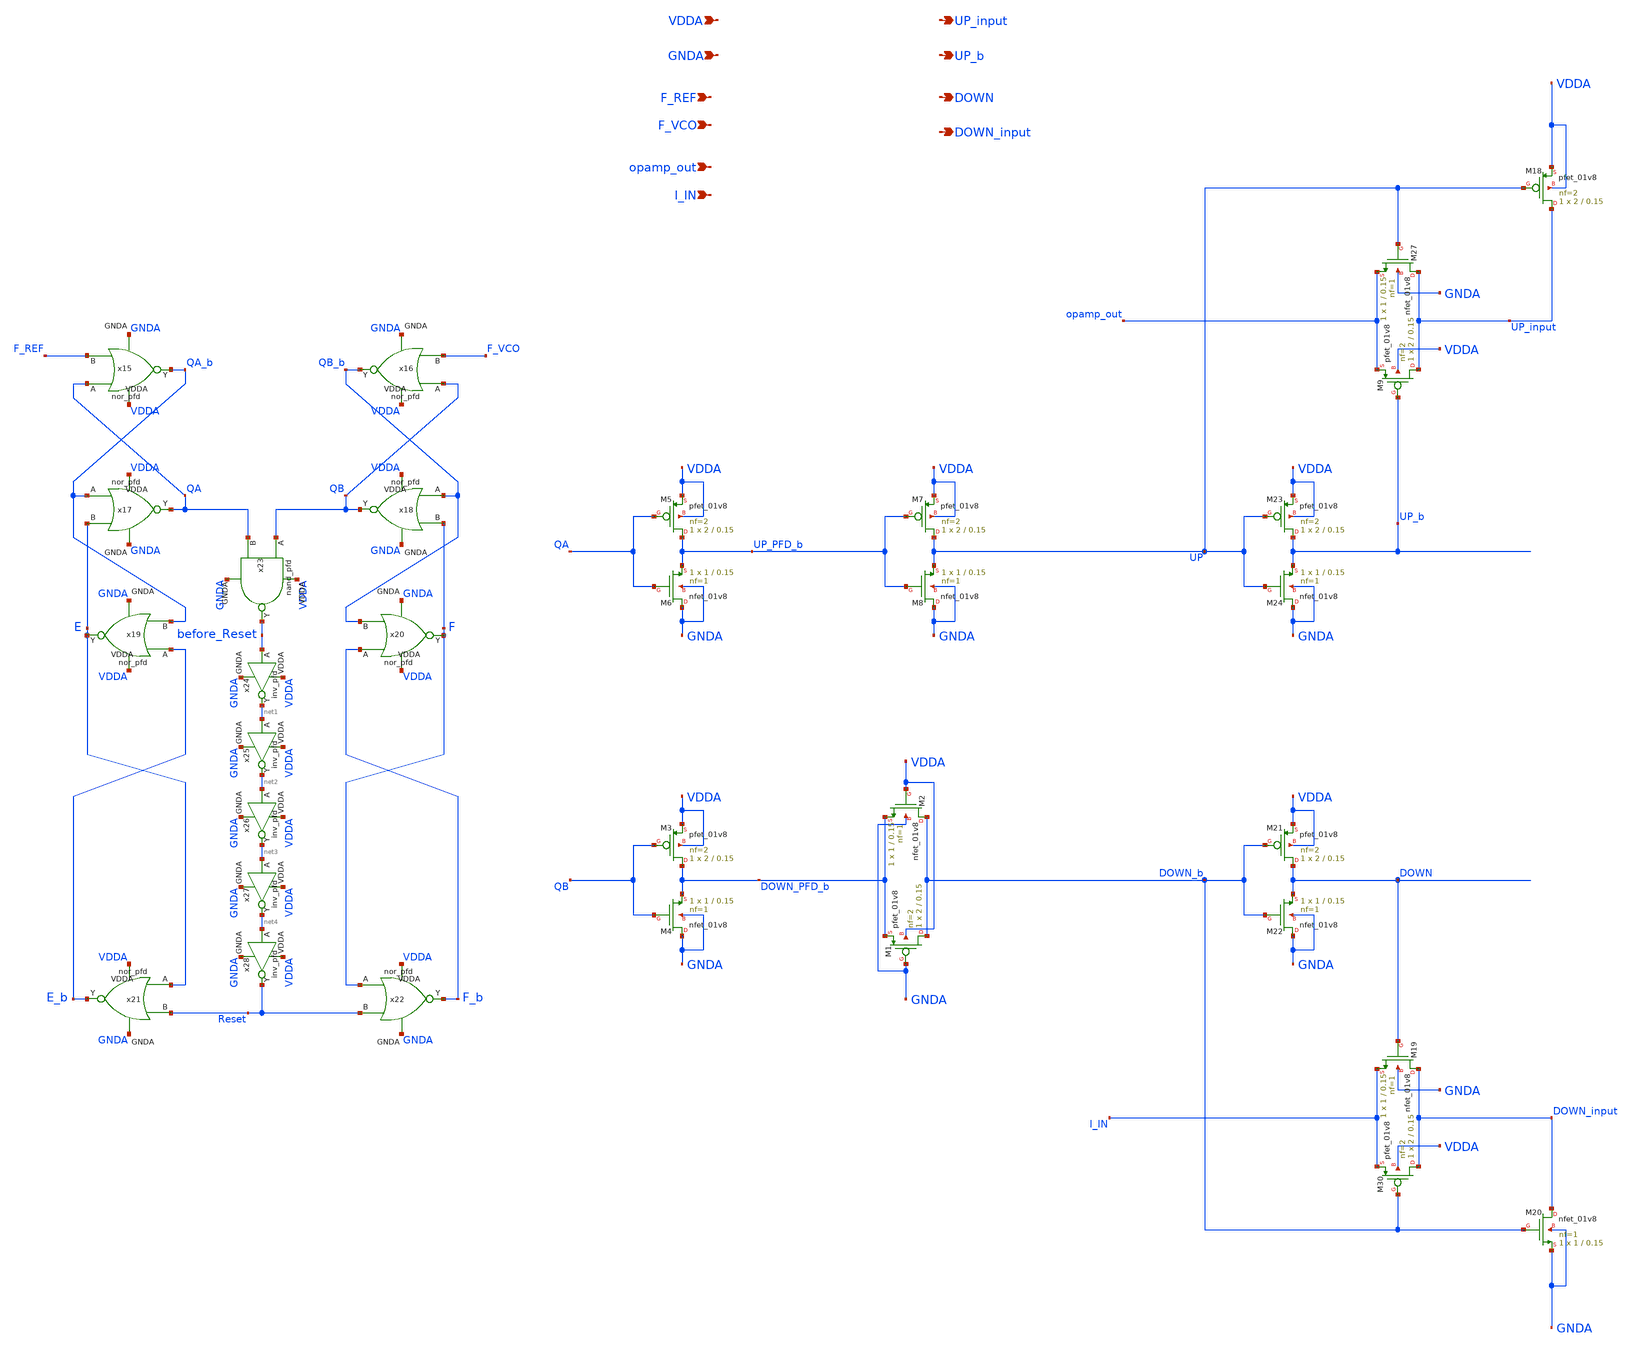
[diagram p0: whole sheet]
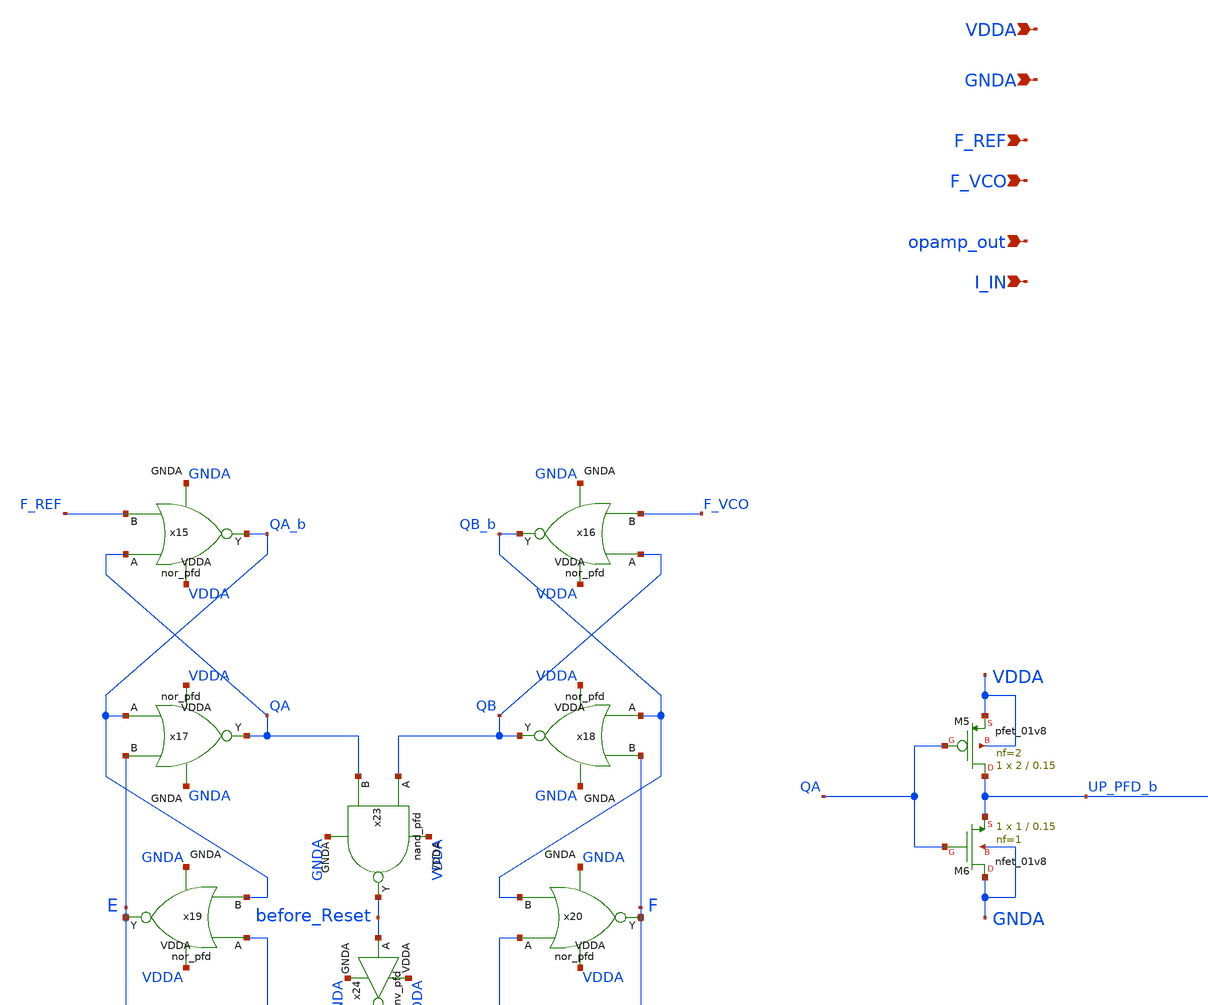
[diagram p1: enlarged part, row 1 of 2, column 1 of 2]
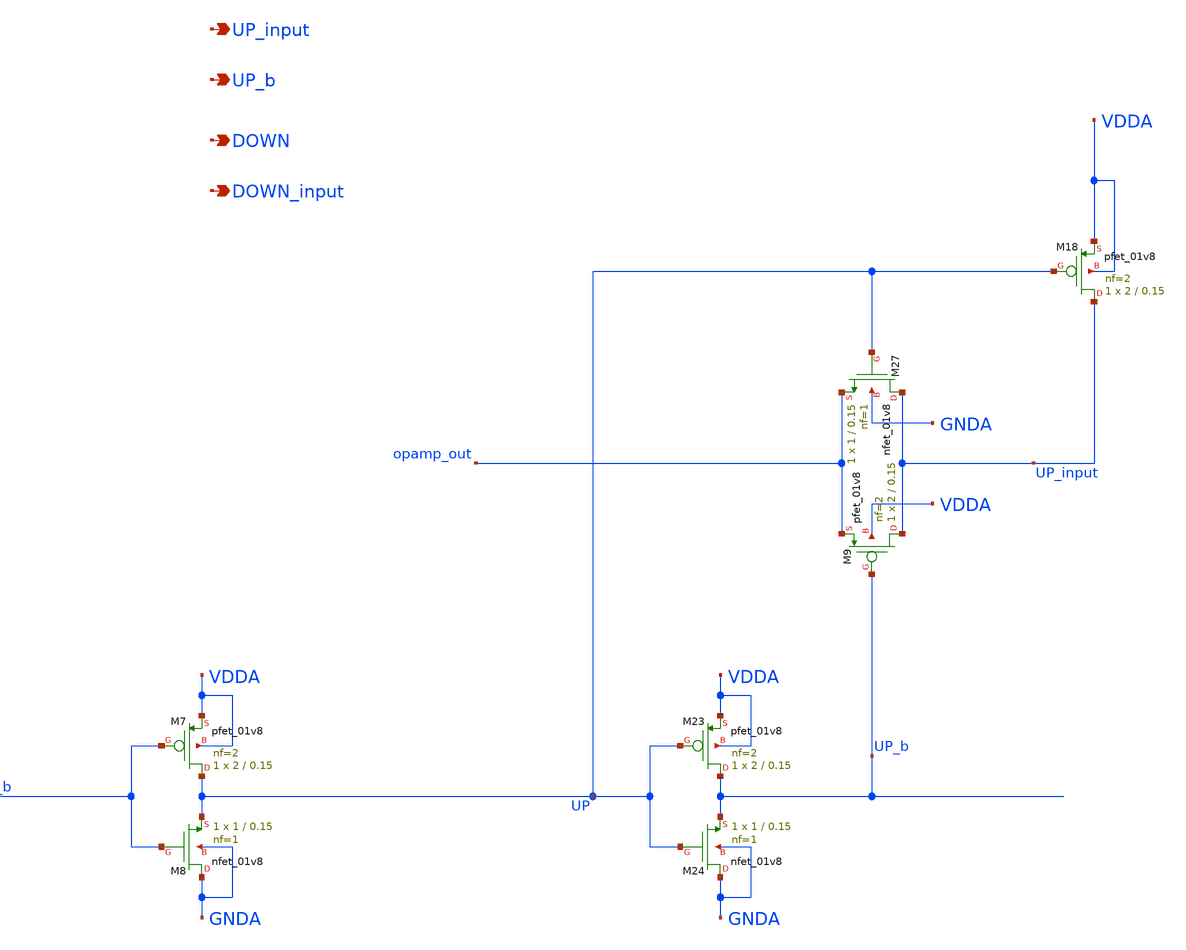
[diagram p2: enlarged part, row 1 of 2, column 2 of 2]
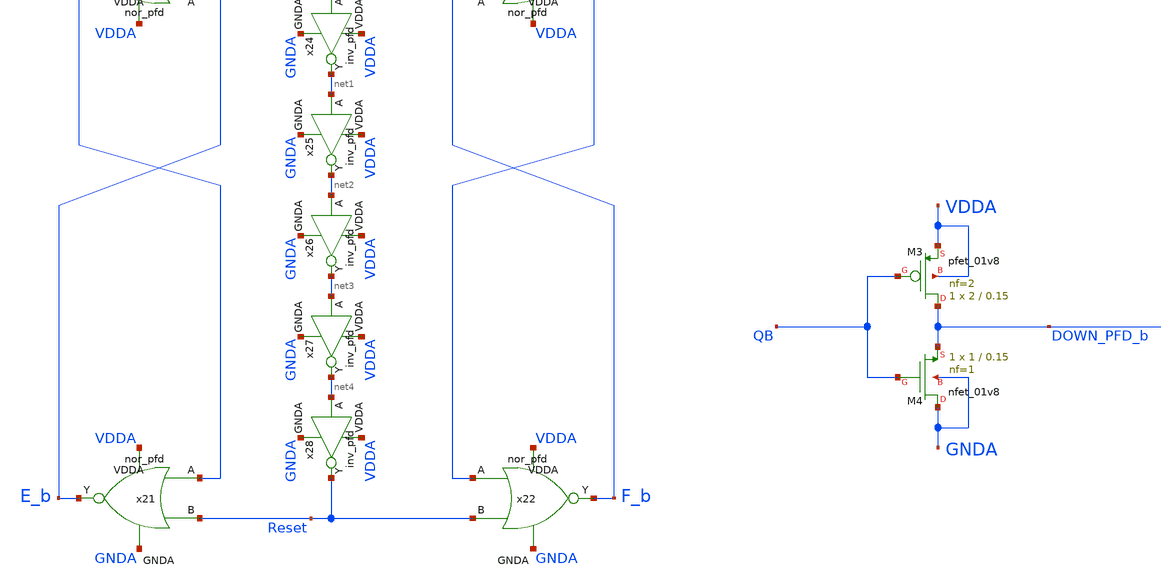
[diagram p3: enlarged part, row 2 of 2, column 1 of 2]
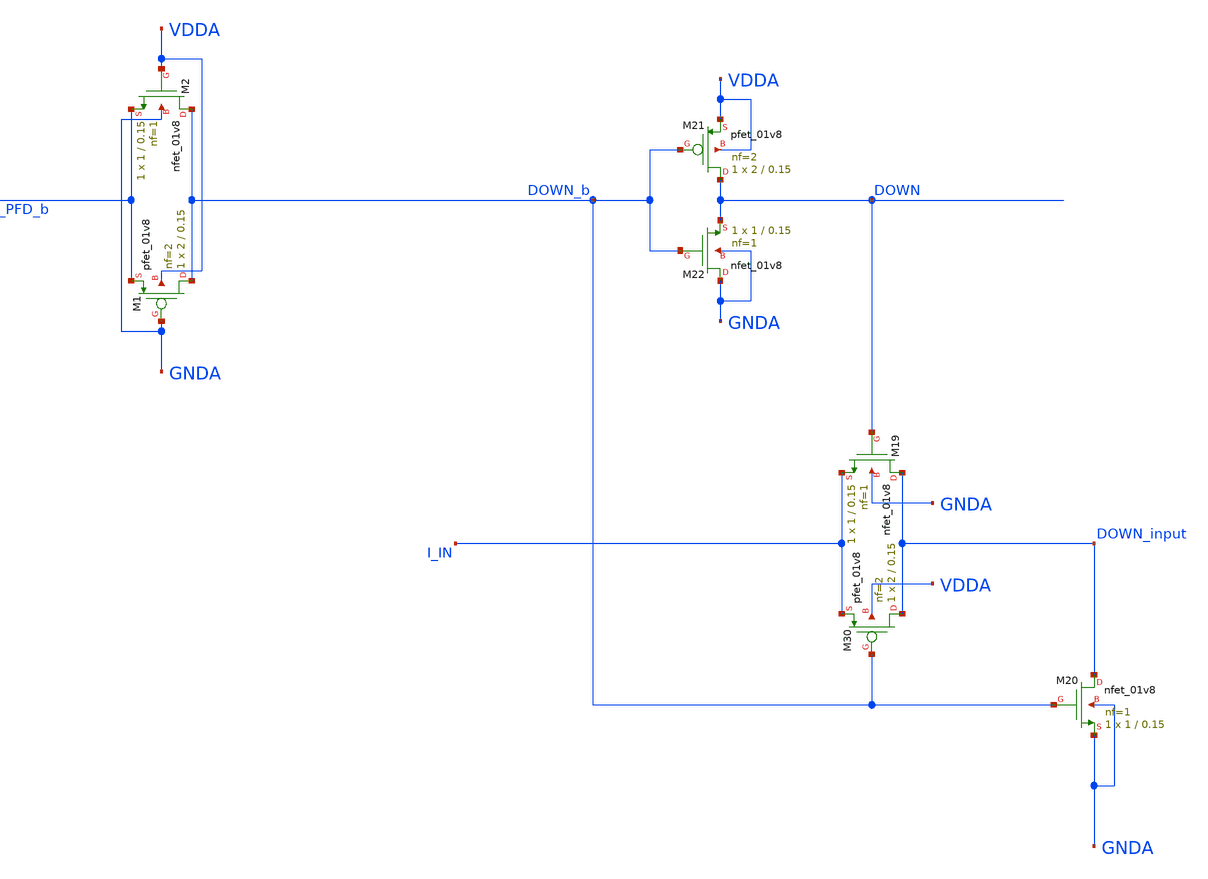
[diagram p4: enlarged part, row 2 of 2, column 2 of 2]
** sch_path: projects/pll/pfd/xschem_ngspice/phase_frequency_detector_6.sch
**.subckt phase_frequency_detector_6 F_REF F_VCO VDDA GNDA UP_input DOWN_input UP_b DOWN opamp_out
*+ I_IN
*.ipin F_REF
*.ipin F_VCO
*.ipin VDDA
*.ipin GNDA
*.opin UP_input
*.opin DOWN_input
*.opin UP_b
*.opin DOWN
*.ipin opamp_out
*.ipin I_IN
XM1 DOWN_b GNDA DOWN_PFD_b VDDA sky130_fd_pr__pfet_01v8 L=0.15 W=2 nf=2 ad='int((nf+1)/2) * W/nf * 0.29'
+ as='int((nf+2)/2) * W/nf * 0.29' pd='2*int((nf+1)/2) * (W/nf + 0.29)' ps='2*int((nf+2)/2) * (W/nf + 0.29)'
+ nrd='0.29 / W' nrs='0.29 / W' sa=0 sb=0 sd=0 mult=1 m=1
XM2 DOWN_b VDDA DOWN_PFD_b GNDA sky130_fd_pr__nfet_01v8 L=0.15 W=1 nf=1 ad='int((nf+1)/2) * W/nf * 0.29'
+ as='int((nf+2)/2) * W/nf * 0.29' pd='2*int((nf+1)/2) * (W/nf + 0.29)' ps='2*int((nf+2)/2) * (W/nf + 0.29)'
+ nrd='0.29 / W' nrs='0.29 / W' sa=0 sb=0 sd=0 mult=1 m=1
XM3 DOWN_PFD_b QB VDDA VDDA sky130_fd_pr__pfet_01v8 L=0.15 W=2 nf=2 ad='int((nf+1)/2) * W/nf * 0.29'
+ as='int((nf+2)/2) * W/nf * 0.29' pd='2*int((nf+1)/2) * (W/nf + 0.29)' ps='2*int((nf+2)/2) * (W/nf + 0.29)'
+ nrd='0.29 / W' nrs='0.29 / W' sa=0 sb=0 sd=0 mult=1 m=1
XM4 GNDA QB DOWN_PFD_b GNDA sky130_fd_pr__nfet_01v8 L=0.15 W=1 nf=1 ad='int((nf+1)/2) * W/nf * 0.29'
+ as='int((nf+2)/2) * W/nf * 0.29' pd='2*int((nf+1)/2) * (W/nf + 0.29)' ps='2*int((nf+2)/2) * (W/nf + 0.29)'
+ nrd='0.29 / W' nrs='0.29 / W' sa=0 sb=0 sd=0 mult=1 m=1
XM5 UP_PFD_b QA VDDA VDDA sky130_fd_pr__pfet_01v8 L=0.15 W=2 nf=2 ad='int((nf+1)/2) * W/nf * 0.29' as='int((nf+2)/2) * W/nf * 0.29'
+ pd='2*int((nf+1)/2) * (W/nf + 0.29)' ps='2*int((nf+2)/2) * (W/nf + 0.29)' nrd='0.29 / W' nrs='0.29 / W'
+ sa=0 sb=0 sd=0 mult=1 m=1
XM6 GNDA QA UP_PFD_b GNDA sky130_fd_pr__nfet_01v8 L=0.15 W=1 nf=1 ad='int((nf+1)/2) * W/nf * 0.29' as='int((nf+2)/2) * W/nf * 0.29'
+ pd='2*int((nf+1)/2) * (W/nf + 0.29)' ps='2*int((nf+2)/2) * (W/nf + 0.29)' nrd='0.29 / W' nrs='0.29 / W'
+ sa=0 sb=0 sd=0 mult=1 m=1
XM7 UP UP_PFD_b VDDA VDDA sky130_fd_pr__pfet_01v8 L=0.15 W=2 nf=2 ad='int((nf+1)/2) * W/nf * 0.29' as='int((nf+2)/2) * W/nf * 0.29'
+ pd='2*int((nf+1)/2) * (W/nf + 0.29)' ps='2*int((nf+2)/2) * (W/nf + 0.29)' nrd='0.29 / W' nrs='0.29 / W'
+ sa=0 sb=0 sd=0 mult=1 m=1
XM8 GNDA UP_PFD_b UP GNDA sky130_fd_pr__nfet_01v8 L=0.15 W=1 nf=1 ad='int((nf+1)/2) * W/nf * 0.29' as='int((nf+2)/2) * W/nf * 0.29'
+ pd='2*int((nf+1)/2) * (W/nf + 0.29)' ps='2*int((nf+2)/2) * (W/nf + 0.29)' nrd='0.29 / W' nrs='0.29 / W'
+ sa=0 sb=0 sd=0 mult=1 m=1
XM9 UP_input UP_b opamp_out VDDA sky130_fd_pr__pfet_01v8 L=0.15 W=2 nf=2 ad='int((nf+1)/2) * W/nf * 0.29'
+ as='int((nf+2)/2) * W/nf * 0.29' pd='2*int((nf+1)/2) * (W/nf + 0.29)' ps='2*int((nf+2)/2) * (W/nf + 0.29)'
+ nrd='0.29 / W' nrs='0.29 / W' sa=0 sb=0 sd=0 mult=1 m=1
XM18 UP_input UP VDDA VDDA sky130_fd_pr__pfet_01v8 L=0.15 W=2 nf=2 ad='int((nf+1)/2) * W/nf * 0.29' as='int((nf+2)/2) * W/nf * 0.29'
+ pd='2*int((nf+1)/2) * (W/nf + 0.29)' ps='2*int((nf+2)/2) * (W/nf + 0.29)' nrd='0.29 / W' nrs='0.29 / W'
+ sa=0 sb=0 sd=0 mult=1 m=1
XM19 DOWN_input DOWN I_IN GNDA sky130_fd_pr__nfet_01v8 L=0.15 W=1 nf=1 ad='int((nf+1)/2) * W/nf * 0.29'
+ as='int((nf+2)/2) * W/nf * 0.29' pd='2*int((nf+1)/2) * (W/nf + 0.29)' ps='2*int((nf+2)/2) * (W/nf + 0.29)'
+ nrd='0.29 / W' nrs='0.29 / W' sa=0 sb=0 sd=0 mult=1 m=1
XM20 DOWN_input DOWN_b GNDA GNDA sky130_fd_pr__nfet_01v8 L=0.15 W=1 nf=1 ad='int((nf+1)/2) * W/nf * 0.29'
+ as='int((nf+2)/2) * W/nf * 0.29' pd='2*int((nf+1)/2) * (W/nf + 0.29)' ps='2*int((nf+2)/2) * (W/nf + 0.29)'
+ nrd='0.29 / W' nrs='0.29 / W' sa=0 sb=0 sd=0 mult=1 m=1
XM21 DOWN DOWN_b VDDA VDDA sky130_fd_pr__pfet_01v8 L=0.15 W=2 nf=2 ad='int((nf+1)/2) * W/nf * 0.29' as='int((nf+2)/2) * W/nf * 0.29'
+ pd='2*int((nf+1)/2) * (W/nf + 0.29)' ps='2*int((nf+2)/2) * (W/nf + 0.29)' nrd='0.29 / W' nrs='0.29 / W'
+ sa=0 sb=0 sd=0 mult=1 m=1
XM22 GNDA DOWN_b DOWN GNDA sky130_fd_pr__nfet_01v8 L=0.15 W=1 nf=1 ad='int((nf+1)/2) * W/nf * 0.29' as='int((nf+2)/2) * W/nf * 0.29'
+ pd='2*int((nf+1)/2) * (W/nf + 0.29)' ps='2*int((nf+2)/2) * (W/nf + 0.29)' nrd='0.29 / W' nrs='0.29 / W'
+ sa=0 sb=0 sd=0 mult=1 m=1
XM23 UP_b UP VDDA VDDA sky130_fd_pr__pfet_01v8 L=0.15 W=2 nf=2 ad='int((nf+1)/2) * W/nf * 0.29' as='int((nf+2)/2) * W/nf * 0.29'
+ pd='2*int((nf+1)/2) * (W/nf + 0.29)' ps='2*int((nf+2)/2) * (W/nf + 0.29)' nrd='0.29 / W' nrs='0.29 / W'
+ sa=0 sb=0 sd=0 mult=1 m=1
XM24 GNDA UP UP_b GNDA sky130_fd_pr__nfet_01v8 L=0.15 W=1 nf=1 ad='int((nf+1)/2) * W/nf * 0.29' as='int((nf+2)/2) * W/nf * 0.29'
+ pd='2*int((nf+1)/2) * (W/nf + 0.29)' ps='2*int((nf+2)/2) * (W/nf + 0.29)' nrd='0.29 / W' nrs='0.29 / W'
+ sa=0 sb=0 sd=0 mult=1 m=1
XM27 UP_input UP opamp_out GNDA sky130_fd_pr__nfet_01v8 L=0.15 W=1 nf=1 ad='int((nf+1)/2) * W/nf * 0.29'
+ as='int((nf+2)/2) * W/nf * 0.29' pd='2*int((nf+1)/2) * (W/nf + 0.29)' ps='2*int((nf+2)/2) * (W/nf + 0.29)'
+ nrd='0.29 / W' nrs='0.29 / W' sa=0 sb=0 sd=0 mult=1 m=1
XM30 DOWN_input DOWN_b I_IN VDDA sky130_fd_pr__pfet_01v8 L=0.15 W=2 nf=2 ad='int((nf+1)/2) * W/nf * 0.29'
+ as='int((nf+2)/2) * W/nf * 0.29' pd='2*int((nf+1)/2) * (W/nf + 0.29)' ps='2*int((nf+2)/2) * (W/nf + 0.29)'
+ nrd='0.29 / W' nrs='0.29 / W' sa=0 sb=0 sd=0 mult=1 m=1
x15 VDDA GNDA QA F_REF QA_b nor_pfd
x16 VDDA GNDA QB F_VCO QB_b nor_pfd
x17 VDDA GNDA QA_b E QA nor_pfd
x18 VDDA GNDA QB_b F QB nor_pfd
x19 VDDA GNDA E_b QA_b E nor_pfd
x20 VDDA GNDA F_b QB_b F nor_pfd
x21 VDDA GNDA E Reset E_b nor_pfd
x22 VDDA GNDA F Reset F_b nor_pfd
x23 VDDA GNDA QB QA before_Reset nand_pfd
x24 VDDA GNDA before_Reset net1 inv_pfd
x25 VDDA GNDA net1 net2 inv_pfd
x26 VDDA GNDA net2 net3 inv_pfd
x27 VDDA GNDA net3 net4 inv_pfd
x28 VDDA GNDA net4 Reset inv_pfd
**.ends

* expanding   symbol:  /foss/designs/my_design/projects/pll/pfd/xschem_ngspice/nor_pfd.sym # of
*+ pins=5
** sym_path: projects/pll/pfd/xschem_ngspice/nor_pfd.sym
** sch_path: projects/pll/pfd/xschem_ngspice/nor_pfd.sch
.subckt nor_pfd VDDA GNDA A B Y
*.ipin A
*.opin Y
*.ipin VDDA
*.ipin GNDA
*.ipin B
XM4 net1 B VDDA VDDA sky130_fd_pr__pfet_01v8 L=0.15 W=2 nf=1 ad='int((nf+1)/2) * W/nf * 0.29' as='int((nf+2)/2) * W/nf * 0.29'
+ pd='2*int((nf+1)/2) * (W/nf + 0.29)' ps='2*int((nf+2)/2) * (W/nf + 0.29)' nrd='0.29 / W' nrs='0.29 / W'
+ sa=0 sb=0 sd=0 mult=1 m=1
XM2 GNDA B Y GNDA sky130_fd_pr__nfet_01v8 L=0.15 W=1 nf=1 ad='int((nf+1)/2) * W/nf * 0.29' as='int((nf+2)/2) * W/nf * 0.29'
+ pd='2*int((nf+1)/2) * (W/nf + 0.29)' ps='2*int((nf+2)/2) * (W/nf + 0.29)' nrd='0.29 / W' nrs='0.29 / W'
+ sa=0 sb=0 sd=0 mult=1 m=1
XM1 GNDA A Y GNDA sky130_fd_pr__nfet_01v8 L=0.15 W=1 nf=1 ad='int((nf+1)/2) * W/nf * 0.29' as='int((nf+2)/2) * W/nf * 0.29'
+ pd='2*int((nf+1)/2) * (W/nf + 0.29)' ps='2*int((nf+2)/2) * (W/nf + 0.29)' nrd='0.29 / W' nrs='0.29 / W'
+ sa=0 sb=0 sd=0 mult=1 m=1
XM3 Y A net1 VDDA sky130_fd_pr__pfet_01v8 L=0.15 W=2 nf=1 ad='int((nf+1)/2) * W/nf * 0.29' as='int((nf+2)/2) * W/nf * 0.29'
+ pd='2*int((nf+1)/2) * (W/nf + 0.29)' ps='2*int((nf+2)/2) * (W/nf + 0.29)' nrd='0.29 / W' nrs='0.29 / W'
+ sa=0 sb=0 sd=0 mult=1 m=1
.ends


* expanding   symbol:  /foss/designs/my_design/projects/pll/pfd/xschem_ngspice/nand_pfd.sym # of
*+ pins=5
** sym_path: projects/pll/pfd/xschem_ngspice/nand_pfd.sym
** sch_path: projects/pll/pfd/xschem_ngspice/nand_pfd.sch
.subckt nand_pfd VDDA GNDA A B Y
*.ipin A
*.opin Y
*.ipin VDDA
*.ipin GNDA
*.ipin B
XM4 Y B VDDA VDDA sky130_fd_pr__pfet_01v8 L=0.15 W=1 nf=2 ad='int((nf+1)/2) * W/nf * 0.29' as='int((nf+2)/2) * W/nf * 0.29'
+ pd='2*int((nf+1)/2) * (W/nf + 0.29)' ps='2*int((nf+2)/2) * (W/nf + 0.29)' nrd='0.29 / W' nrs='0.29 / W'
+ sa=0 sb=0 sd=0 mult=1 m=1
XM2 net1 B Y GNDA sky130_fd_pr__nfet_01v8 L=0.15 W=0.5 nf=1 ad='int((nf+1)/2) * W/nf * 0.29' as='int((nf+2)/2) * W/nf * 0.29'
+ pd='2*int((nf+1)/2) * (W/nf + 0.29)' ps='2*int((nf+2)/2) * (W/nf + 0.29)' nrd='0.29 / W' nrs='0.29 / W'
+ sa=0 sb=0 sd=0 mult=1 m=1
XM1 GNDA A net1 GNDA sky130_fd_pr__nfet_01v8 L=0.15 W=0.5 nf=1 ad='int((nf+1)/2) * W/nf * 0.29' as='int((nf+2)/2) * W/nf * 0.29'
+ pd='2*int((nf+1)/2) * (W/nf + 0.29)' ps='2*int((nf+2)/2) * (W/nf + 0.29)' nrd='0.29 / W' nrs='0.29 / W'
+ sa=0 sb=0 sd=0 mult=1 m=1
XM3 Y A VDDA VDDA sky130_fd_pr__pfet_01v8 L=0.15 W=1 nf=2 ad='int((nf+1)/2) * W/nf * 0.29' as='int((nf+2)/2) * W/nf * 0.29'
+ pd='2*int((nf+1)/2) * (W/nf + 0.29)' ps='2*int((nf+2)/2) * (W/nf + 0.29)' nrd='0.29 / W' nrs='0.29 / W'
+ sa=0 sb=0 sd=0 mult=1 m=1
.ends


* expanding   symbol:  /foss/designs/my_design/projects/pll/pfd/xschem_ngspice/inv_pfd.sym # of
*+ pins=4
** sym_path: projects/ASU/EEE572/schematic/inv_pfd.sym
** sch_path: projects/ASU/EEE572/schematic/inv_pfd.sch
.subckt inv_pfd VDDA GNDA A Y
*.ipin A
*.opin Y
*.ipin VDDA
*.ipin GNDA
XM2 Y A VDDA VDDA sky130_fd_pr__pfet_01v8 L=0.15 W=2 nf=1 ad='int((nf+1)/2) * W/nf * 0.29' as='int((nf+2)/2) * W/nf * 0.29'
+ pd='2*int((nf+1)/2) * (W/nf + 0.29)' ps='2*int((nf+2)/2) * (W/nf + 0.29)' nrd='0.29 / W' nrs='0.29 / W'
+ sa=0 sb=0 sd=0 mult=1 m=1
XM1 GNDA A Y GNDA sky130_fd_pr__nfet_01v8 L=0.15 W=1 nf=1 ad='int((nf+1)/2) * W/nf * 0.29' as='int((nf+2)/2) * W/nf * 0.29'
+ pd='2*int((nf+1)/2) * (W/nf + 0.29)' ps='2*int((nf+2)/2) * (W/nf + 0.29)' nrd='0.29 / W' nrs='0.29 / W'
+ sa=0 sb=0 sd=0 mult=1 m=1
.ends

.end
